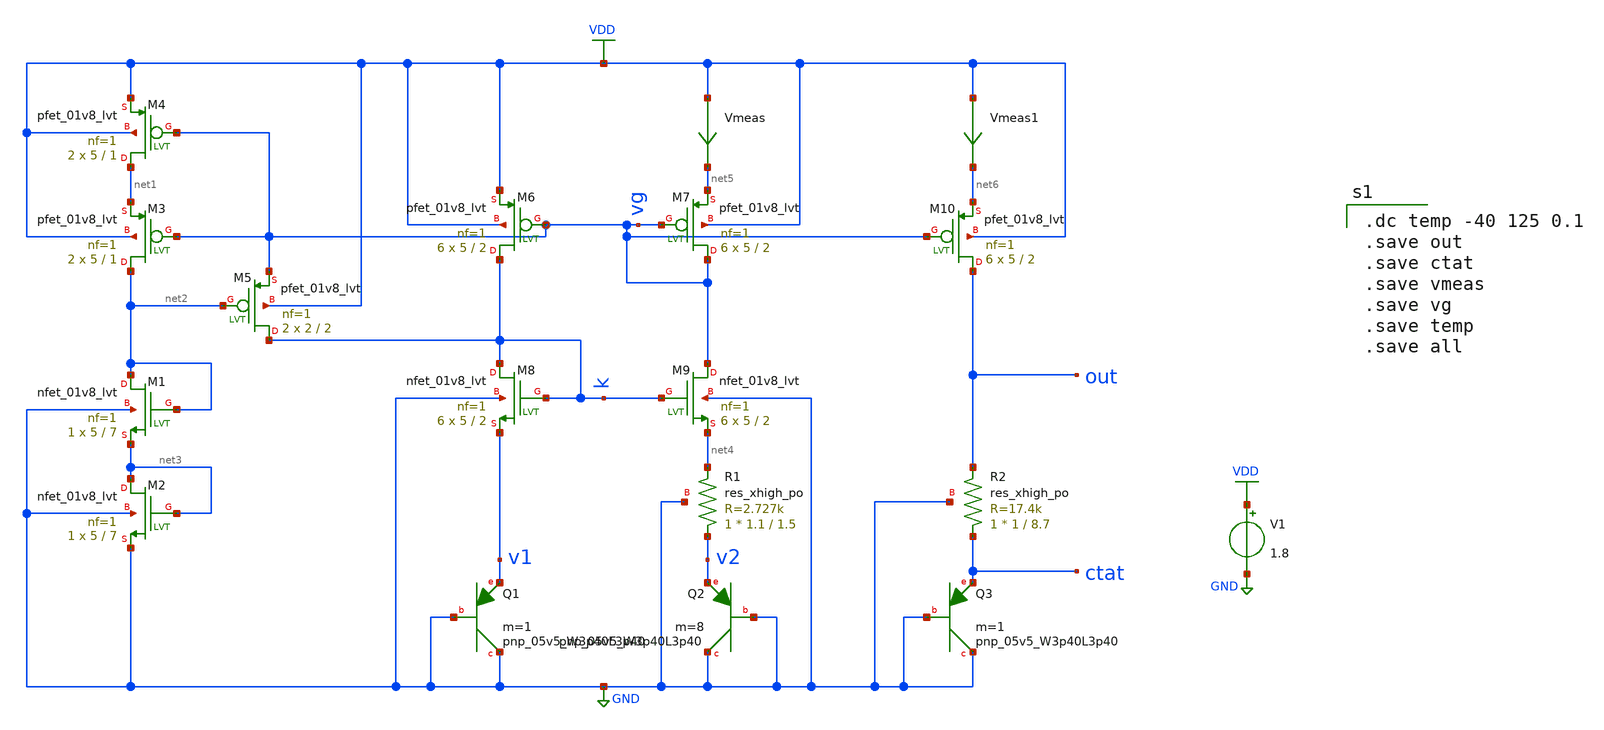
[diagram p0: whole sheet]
** sch_path: ANOTHER_SOLUTIONS_CONSIDERED/ANOTHER_BIAS_FOR_TEMPERATURE_SENSOR/BGR/XSCHEM/BGR_lvt_design_tb.sch
**.subckt BGR_lvt_design_tb
V1 VDD GND 1.8
XM1 net2 net2 net3 GND sky130_fd_pr__nfet_01v8_lvt L=7 W=5 nf=1 ad='int((nf+1)/2) * W/nf * 0.29' as='int((nf+2)/2) * W/nf * 0.29'
+ pd='2*int((nf+1)/2) * (W/nf + 0.29)' ps='2*int((nf+2)/2) * (W/nf + 0.29)' nrd='0.29 / W' nrs='0.29 / W'
+ sa=0 sb=0 sd=0 mult=1 m=1
XM2 net3 net3 GND GND sky130_fd_pr__nfet_01v8_lvt L=7 W=5 nf=1 ad='int((nf+1)/2) * W/nf * 0.29' as='int((nf+2)/2) * W/nf * 0.29'
+ pd='2*int((nf+1)/2) * (W/nf + 0.29)' ps='2*int((nf+2)/2) * (W/nf + 0.29)' nrd='0.29 / W' nrs='0.29 / W'
+ sa=0 sb=0 sd=0 mult=1 m=1
XM3 net2 vg net1 VDD sky130_fd_pr__pfet_01v8_lvt L=1 W=5 nf=1 ad='int((nf+1)/2) * W/nf * 0.29' as='int((nf+2)/2) * W/nf * 0.29'
+ pd='2*int((nf+1)/2) * (W/nf + 0.29)' ps='2*int((nf+2)/2) * (W/nf + 0.29)' nrd='0.29 / W' nrs='0.29 / W'
+ sa=0 sb=0 sd=0 mult=2 m=2
XM4 net1 vg VDD VDD sky130_fd_pr__pfet_01v8_lvt L=1 W=5 nf=1 ad='int((nf+1)/2) * W/nf * 0.29' as='int((nf+2)/2) * W/nf * 0.29'
+ pd='2*int((nf+1)/2) * (W/nf + 0.29)' ps='2*int((nf+2)/2) * (W/nf + 0.29)' nrd='0.29 / W' nrs='0.29 / W'
+ sa=0 sb=0 sd=0 mult=2 m=2
XM5 k net2 vg VDD sky130_fd_pr__pfet_01v8_lvt L=2 W=2 nf=1 ad='int((nf+1)/2) * W/nf * 0.29' as='int((nf+2)/2) * W/nf * 0.29'
+ pd='2*int((nf+1)/2) * (W/nf + 0.29)' ps='2*int((nf+2)/2) * (W/nf + 0.29)' nrd='0.29 / W' nrs='0.29 / W'
+ sa=0 sb=0 sd=0 mult=2 m=2
XM6 k vg VDD VDD sky130_fd_pr__pfet_01v8_lvt L=2 W=5 nf=1 ad='int((nf+1)/2) * W/nf * 0.29' as='int((nf+2)/2) * W/nf * 0.29'
+ pd='2*int((nf+1)/2) * (W/nf + 0.29)' ps='2*int((nf+2)/2) * (W/nf + 0.29)' nrd='0.29 / W' nrs='0.29 / W'
+ sa=0 sb=0 sd=0 mult=6 m=6
XM7 vg vg net5 VDD sky130_fd_pr__pfet_01v8_lvt L=2 W=5 nf=1 ad='int((nf+1)/2) * W/nf * 0.29' as='int((nf+2)/2) * W/nf * 0.29'
+ pd='2*int((nf+1)/2) * (W/nf + 0.29)' ps='2*int((nf+2)/2) * (W/nf + 0.29)' nrd='0.29 / W' nrs='0.29 / W'
+ sa=0 sb=0 sd=0 mult=6 m=6
XM8 k k v1 GND sky130_fd_pr__nfet_01v8_lvt L=2 W=5 nf=1 ad='int((nf+1)/2) * W/nf * 0.29' as='int((nf+2)/2) * W/nf * 0.29'
+ pd='2*int((nf+1)/2) * (W/nf + 0.29)' ps='2*int((nf+2)/2) * (W/nf + 0.29)' nrd='0.29 / W' nrs='0.29 / W'
+ sa=0 sb=0 sd=0 mult=6 m=6
XM9 vg k net4 GND sky130_fd_pr__nfet_01v8_lvt L=2 W=5 nf=1 ad='int((nf+1)/2) * W/nf * 0.29' as='int((nf+2)/2) * W/nf * 0.29'
+ pd='2*int((nf+1)/2) * (W/nf + 0.29)' ps='2*int((nf+2)/2) * (W/nf + 0.29)' nrd='0.29 / W' nrs='0.29 / W'
+ sa=0 sb=0 sd=0 mult=6 m=6
XQ1 GND GND v1 sky130_fd_pr__pnp_05v5_W3p40L3p40 m=1
XR1 v2 net4 GND sky130_fd_pr__res_xhigh_po W=1.1 L=1.5 mult=1 m=1
XQ2 GND GND v2 sky130_fd_pr__pnp_05v5_W3p40L3p40 m=8
XM10 out vg net6 VDD sky130_fd_pr__pfet_01v8_lvt L=2 W=5 nf=1 ad='int((nf+1)/2) * W/nf * 0.29' as='int((nf+2)/2) * W/nf * 0.29'
+ pd='2*int((nf+1)/2) * (W/nf + 0.29)' ps='2*int((nf+2)/2) * (W/nf + 0.29)' nrd='0.29 / W' nrs='0.29 / W'
+ sa=0 sb=0 sd=0 mult=6 m=6
XR2 ctat out GND sky130_fd_pr__res_xhigh_po W=1 L=8.7 mult=1 m=1
XQ3 GND GND ctat sky130_fd_pr__pnp_05v5_W3p40L3p40 m=1
Vmeas VDD net5 0
.save i(vmeas)
Vmeas1 VDD net6 0
.save i(vmeas1)
**** begin user architecture code

.dc temp -40 125 0.1
.save out
.save ctat
.save vmeas
.save vg
.save temp
.save all


** opencircuitdesign pdks install
.lib $::SKYWATER_MODELS/sky130.lib.spice tt


**** end user architecture code
**.ends
.GLOBAL VDD
.GLOBAL GND
.end
